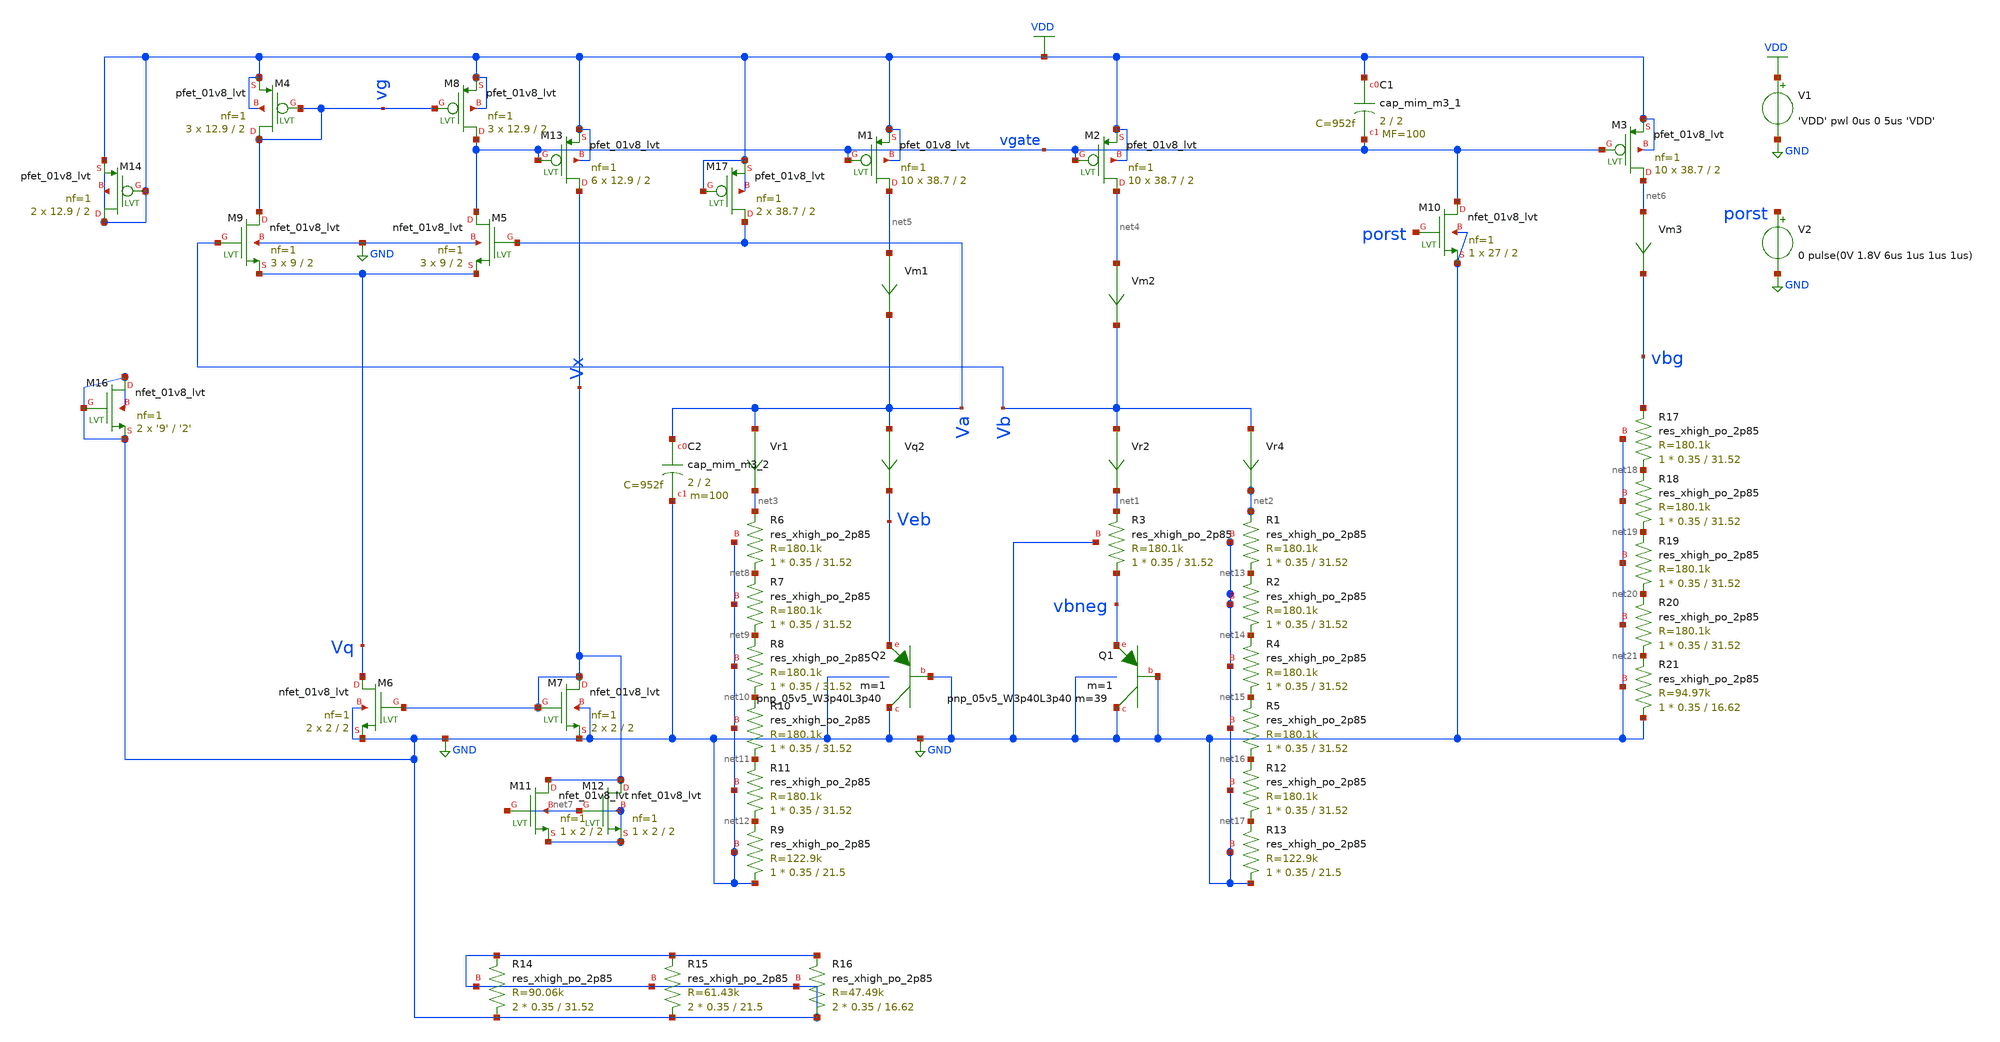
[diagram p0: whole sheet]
** sch_path: schematics/tsmc_bandgap_real_op_layout.sch
**.subckt tsmc_bandgap_real_op_layout
V1 VDD GND 'VDD' pwl 0us 0 5us 'VDD'
XQ2 GND GND Veb sky130_fd_pr__pnp_05v5_W3p40L3p40 m=1
Vr4 Vb net2 0
.save i(vr4)
Vr2 Vb net1 0
.save i(vr2)
Vm1 net5 Va 0
.save i(vm1)
Vm2 net4 Vb 0
.save i(vm2)
Vm3 net6 vbg 0
.save i(vm3)
Vr1 Va net3 0
.save i(vr1)
Vq2 Va Veb 0
.save i(vq2)
XQ1 GND GND vbneg sky130_fd_pr__pnp_05v5_W3p40L3p40 m=39 m=1
XM5 vgate Va Vq GND sky130_fd_pr__nfet_01v8_lvt L=2 W=9 nf=1 ad='int((nf+1)/2) * W/nf * 0.29' as='int((nf+2)/2) * W/nf * 0.29'
+ pd='2*int((nf+1)/2) * (W/nf + 0.29)' ps='2*int((nf+2)/2) * (W/nf + 0.29)' nrd='0.29 / W' nrs='0.29 / W'
+ sa=0 sb=0 sd=0 mult=3 m=3
XM6 Vq Vx GND GND sky130_fd_pr__nfet_01v8_lvt L=2 W=2 nf=1 ad='int((nf+1)/2) * W/nf * 0.29' as='int((nf+2)/2) * W/nf * 0.29'
+ pd='2*int((nf+1)/2) * (W/nf + 0.29)' ps='2*int((nf+2)/2) * (W/nf + 0.29)' nrd='0.29 / W' nrs='0.29 / W'
+ sa=0 sb=0 sd=0 mult=2 m=2
XM9 vg Vb Vq GND sky130_fd_pr__nfet_01v8_lvt L=2 W=9 nf=1 ad='int((nf+1)/2) * W/nf * 0.29' as='int((nf+2)/2) * W/nf * 0.29'
+ pd='2*int((nf+1)/2) * (W/nf + 0.29)' ps='2*int((nf+2)/2) * (W/nf + 0.29)' nrd='0.29 / W' nrs='0.29 / W'
+ sa=0 sb=0 sd=0 mult=3 m=3
XM7 Vx Vx GND GND sky130_fd_pr__nfet_01v8_lvt L=2 W=2 nf=1 ad='int((nf+1)/2) * W/nf * 0.29' as='int((nf+2)/2) * W/nf * 0.29'
+ pd='2*int((nf+1)/2) * (W/nf + 0.29)' ps='2*int((nf+2)/2) * (W/nf + 0.29)' nrd='0.29 / W' nrs='0.29 / W'
+ sa=0 sb=0 sd=0 mult=2 m=2
XM13 Vx vgate VDD VDD sky130_fd_pr__pfet_01v8_lvt L=2 W=12.9 nf=1 ad='int((nf+1)/2) * W/nf * 0.29' as='int((nf+2)/2) * W/nf * 0.29'
+ pd='2*int((nf+1)/2) * (W/nf + 0.29)' ps='2*int((nf+2)/2) * (W/nf + 0.29)' nrd='0.29 / W' nrs='0.29 / W'
+ sa=0 sb=0 sd=0 mult=6 m=6
XM1 net5 vgate VDD VDD sky130_fd_pr__pfet_01v8_lvt L=2 W=38.7 nf=1 ad='int((nf+1)/2) * W/nf * 0.29' as='int((nf+2)/2) * W/nf * 0.29'
+ pd='2*int((nf+1)/2) * (W/nf + 0.29)' ps='2*int((nf+2)/2) * (W/nf + 0.29)' nrd='0.29 / W' nrs='0.29 / W'
+ sa=0 sb=0 sd=0 mult=10 m=10
XM2 net4 vgate VDD VDD sky130_fd_pr__pfet_01v8_lvt L=2 W=38.7 nf=1 ad='int((nf+1)/2) * W/nf * 0.29' as='int((nf+2)/2) * W/nf * 0.29'
+ pd='2*int((nf+1)/2) * (W/nf + 0.29)' ps='2*int((nf+2)/2) * (W/nf + 0.29)' nrd='0.29 / W' nrs='0.29 / W'
+ sa=0 sb=0 sd=0 mult=10 m=10
XM3 net6 vgate VDD VDD sky130_fd_pr__pfet_01v8_lvt L=2 W=38.7 nf=1 ad='int((nf+1)/2) * W/nf * 0.29' as='int((nf+2)/2) * W/nf * 0.29'
+ pd='2*int((nf+1)/2) * (W/nf + 0.29)' ps='2*int((nf+2)/2) * (W/nf + 0.29)' nrd='0.29 / W' nrs='0.29 / W'
+ sa=0 sb=0 sd=0 mult=10 m=10
XM4 vg vg VDD VDD sky130_fd_pr__pfet_01v8_lvt L=2 W=12.9 nf=1 ad='int((nf+1)/2) * W/nf * 0.29' as='int((nf+2)/2) * W/nf * 0.29'
+ pd='2*int((nf+1)/2) * (W/nf + 0.29)' ps='2*int((nf+2)/2) * (W/nf + 0.29)' nrd='0.29 / W' nrs='0.29 / W'
+ sa=0 sb=0 sd=0 mult=3 m=3
XM8 vgate vg VDD VDD sky130_fd_pr__pfet_01v8_lvt L=2 W=12.9 nf=1 ad='int((nf+1)/2) * W/nf * 0.29' as='int((nf+2)/2) * W/nf * 0.29'
+ pd='2*int((nf+1)/2) * (W/nf + 0.29)' ps='2*int((nf+2)/2) * (W/nf + 0.29)' nrd='0.29 / W' nrs='0.29 / W'
+ sa=0 sb=0 sd=0 mult=3 m=3
XM10 vgate porst GND GND sky130_fd_pr__nfet_01v8_lvt L=2 W=27 nf=1 ad='int((nf+1)/2) * W/nf * 0.29' as='int((nf+2)/2) * W/nf * 0.29'
+ pd='2*int((nf+1)/2) * (W/nf + 0.29)' ps='2*int((nf+2)/2) * (W/nf + 0.29)' nrd='0.29 / W' nrs='0.29 / W'
+ sa=0 sb=0 sd=0 mult=1 m=1
V2 porst GND 0 pulse(0V 1.8V 6us 1us 1us 1us)
XR6 net8 net3 GND sky130_fd_pr__res_xhigh_po_2p85 L=31.52 mult=1 m=1
XR7 net9 net8 GND sky130_fd_pr__res_xhigh_po_2p85 L=31.52 mult=1 m=1
XR8 net10 net9 GND sky130_fd_pr__res_xhigh_po_2p85 L=31.52 mult=1 m=1
XR10 net11 net10 GND sky130_fd_pr__res_xhigh_po_2p85 L=31.52 mult=1 m=1
XR11 net12 net11 GND sky130_fd_pr__res_xhigh_po_2p85 L=31.52 mult=1 m=1
XR9 GND net12 GND sky130_fd_pr__res_xhigh_po_2p85 L=21.5 mult=1 m=1
XR3 vbneg net1 GND sky130_fd_pr__res_xhigh_po_2p85 L=31.52 mult=1 m=1
XR1 net13 net2 GND sky130_fd_pr__res_xhigh_po_2p85 L=31.52 mult=1 m=1
XR2 net14 net13 GND sky130_fd_pr__res_xhigh_po_2p85 L=31.52 mult=1 m=1
XR4 net15 net14 GND sky130_fd_pr__res_xhigh_po_2p85 L=31.52 mult=1 m=1
XR5 net16 net15 GND sky130_fd_pr__res_xhigh_po_2p85 L=31.52 mult=1 m=1
XR12 net17 net16 GND sky130_fd_pr__res_xhigh_po_2p85 L=31.52 mult=1 m=1
XR13 GND net17 GND sky130_fd_pr__res_xhigh_po_2p85 L=21.5 mult=1 m=1
XR17 net18 vbg GND sky130_fd_pr__res_xhigh_po_2p85 L=31.52 mult=1 m=1
XR18 net19 net18 GND sky130_fd_pr__res_xhigh_po_2p85 L=31.52 mult=1 m=1
XR19 net20 net19 GND sky130_fd_pr__res_xhigh_po_2p85 L=31.52 mult=1 m=1
XR20 net21 net20 GND sky130_fd_pr__res_xhigh_po_2p85 L=31.52 mult=1 m=1
XR21 GND net21 GND sky130_fd_pr__res_xhigh_po_2p85 L=16.62 mult=1 m=1
XC1 VDD vgate sky130_fd_pr__cap_mim_m3_1 W=2 L=2 MF=100 m=100
XC2 Va GND sky130_fd_pr__cap_mim_m3_2 W=2 L=2 MF=100 m=100
XR14 GND GND GND sky130_fd_pr__res_xhigh_po_2p85 L=31.52 mult=2 m=2
XR15 GND GND GND sky130_fd_pr__res_xhigh_po_2p85 L=21.5 mult=2 m=2
XR16 GND GND GND sky130_fd_pr__res_xhigh_po_2p85 L=16.62 mult=2 m=2
XM11 Vx net7 net7 net7 sky130_fd_pr__nfet_01v8_lvt L=2 W=2 nf=1 ad='int((nf+1)/2) * W/nf * 0.29' as='int((nf+2)/2) * W/nf * 0.29'
+ pd='2*int((nf+1)/2) * (W/nf + 0.29)' ps='2*int((nf+2)/2) * (W/nf + 0.29)' nrd='0.29 / W' nrs='0.29 / W'
+ sa=0 sb=0 sd=0 mult=1 m=1
XM12 Vx net7 net7 net7 sky130_fd_pr__nfet_01v8_lvt L=2 W=2 nf=1 ad='int((nf+1)/2) * W/nf * 0.29' as='int((nf+2)/2) * W/nf * 0.29'
+ pd='2*int((nf+1)/2) * (W/nf + 0.29)' ps='2*int((nf+2)/2) * (W/nf + 0.29)' nrd='0.29 / W' nrs='0.29 / W'
+ sa=0 sb=0 sd=0 mult=1 m=1
XM14 VDD VDD VDD VDD sky130_fd_pr__pfet_01v8_lvt L=2 W=12.9 nf=1 ad='int((nf+1)/2) * W/nf * 0.29' as='int((nf+2)/2) * W/nf * 0.29'
+ pd='2*int((nf+1)/2) * (W/nf + 0.29)' ps='2*int((nf+2)/2) * (W/nf + 0.29)' nrd='0.29 / W' nrs='0.29 / W'
+ sa=0 sb=0 sd=0 mult=2 m=2
XM16 GND GND GND GND sky130_fd_pr__nfet_01v8_lvt L='2' W='9' nf=1 ad='int((nf+1)/2) * W/nf * 0.29' as='int((nf+2)/2) * W/nf * 0.29'
+ pd='2*int((nf+1)/2) * (W/nf + 0.29)' ps='2*int((nf+2)/2) * (W/nf + 0.29)' nrd='0.29 / W' nrs='0.29 / W'
+ sa=0 sb=0 sd=0 mult=2 m=2
XM17 Va VDD VDD VDD sky130_fd_pr__pfet_01v8_lvt L=2 W=38.7 nf=1 ad='int((nf+1)/2) * W/nf * 0.29' as='int((nf+2)/2) * W/nf * 0.29'
+ pd='2*int((nf+1)/2) * (W/nf + 0.29)' ps='2*int((nf+2)/2) * (W/nf + 0.29)' nrd='0.29 / W' nrs='0.29 / W'
+ sa=0 sb=0 sd=0 mult=2 m=2
**** begin user architecture code

.include $::SKYWATER_MODELS/cells/nfet_01v8/sky130_fd_pr__nfet_01v8__tt.corner.spice
.include $::SKYWATER_MODELS/cells/nfet_01v8_lvt/sky130_fd_pr__nfet_01v8_lvt__tt.corner.spice
.include $::SKYWATER_MODELS/cells/pfet_01v8/sky130_fd_pr__pfet_01v8__tt.corner.spice
.include $::SKYWATER_MODELS/cells/nfet_03v3_nvt/sky130_fd_pr__nfet_03v3_nvt__tt.corner.spice
.include $::SKYWATER_MODELS/cells/nfet_05v0_nvt/sky130_fd_pr__nfet_05v0_nvt__tt.corner.spice
.include $::SKYWATER_MODELS/cells/esd_nfet_01v8/sky130_fd_pr__esd_nfet_01v8__tt.corner.spice
.include $::SKYWATER_MODELS/cells/pfet_01v8_lvt/sky130_fd_pr__pfet_01v8_lvt__tt.corner.spice
.include $::SKYWATER_MODELS/cells/pfet_01v8_hvt/sky130_fd_pr__pfet_01v8_hvt__tt.corner.spice
.include $::SKYWATER_MODELS/cells/esd_pfet_g5v0d10v5/sky130_fd_pr__esd_pfet_g5v0d10v5__tt.corner.spice
.include $::SKYWATER_MODELS/cells/pfet_g5v0d10v5/sky130_fd_pr__pfet_g5v0d10v5__tt.corner.spice
.include $::SKYWATER_MODELS/cells/pfet_g5v0d16v0/sky130_fd_pr__pfet_g5v0d16v0__tt.corner.spice
.include $::SKYWATER_MODELS/cells/nfet_g5v0d10v5/sky130_fd_pr__nfet_g5v0d10v5__tt.corner.spice
.include $::SKYWATER_MODELS/cells/nfet_g5v0d16v0/sky130_fd_pr__nfet_g5v0d16v0__tt_discrete.corner.spice
.include $::SKYWATER_MODELS/cells/esd_nfet_g5v0d10v5/sky130_fd_pr__esd_nfet_g5v0d10v5__tt.corner.spice
.include $::SKYWATER_MODELS/models/corners/tt/nonfet.spice
* Mismatch parameters
.include $::SKYWATER_MODELS/cells/nfet_01v8/sky130_fd_pr__nfet_01v8__mismatch.corner.spice
.include $::SKYWATER_MODELS/cells/pfet_01v8/sky130_fd_pr__pfet_01v8__mismatch.corner.spice
.include $::SKYWATER_MODELS/cells/nfet_01v8_lvt/sky130_fd_pr__nfet_01v8_lvt__mismatch.corner.spice
.include $::SKYWATER_MODELS/cells/pfet_01v8_lvt/sky130_fd_pr__pfet_01v8_lvt__mismatch.corner.spice
.include $::SKYWATER_MODELS/cells/pfet_01v8_hvt/sky130_fd_pr__pfet_01v8_hvt__mismatch.corner.spice
.include $::SKYWATER_MODELS/cells/nfet_g5v0d10v5/sky130_fd_pr__nfet_g5v0d10v5__mismatch.corner.spice
.include $::SKYWATER_MODELS/cells/pfet_g5v0d10v5/sky130_fd_pr__pfet_g5v0d10v5__mismatch.corner.spice
.include $::SKYWATER_MODELS/cells/nfet_05v0_nvt/sky130_fd_pr__nfet_05v0_nvt__mismatch.corner.spice
.include $::SKYWATER_MODELS/cells/nfet_03v3_nvt/sky130_fd_pr__nfet_03v3_nvt__mismatch.corner.spice
* Resistor$::SKYWATER_MODELS/Capacitor
.include $::SKYWATER_MODELS/models/r+c/res_typical__cap_typical.spice
.include $::SKYWATER_MODELS/models/r+c/res_typical__cap_typical__lin.spice
* Special cells
.include $::SKYWATER_MODELS/models/corners/tt/specialized_cells.spice
* All models
.include $::SKYWATER_MODELS/models/all.spice
*.include $::SKYWATER_MODELS/cells/pnp_05v5/sky130_fd_pr__pnp_05v5_W3p40L3p40.model.spice
.include /tmp/kustinj/ee272bclone/open_pdks/sky130A/libs.ref/sky130_fd_pr/spice/sky130_fd_pr__pnp_05v5_W3p40L3p40.model.spice
* Corner
.include $::SKYWATER_MODELS/models/corners/tt/rf.spice



.ic V(vgate)=0
.ic V(vg)=0
.option savecurrents
.param mc_mm_switch=0
.param R3val='22.187k'
.param alpha='1'
.param R2R3ratio='5.6555038*alpha'
.param R2val='R3val*R2R3ratio'
.param R4R2ratio='0.79694273'
.param R4val='R2val*R4R2ratio
.param VDD=1.8
.control
save all  @m.xm1.msky130_fd_pr__pfet_01v8_lvt[gm]  @m.xm2.msky130_fd_pr__pfet_01v8_lvt[gm]  @m.xm3.msky130_fd_pr__pfet_01v8_lvt[gm]  @m.xm4.msky130_fd_pr__pfet_01v8_lvt[gm]  @m.xm5.msky130_fd_pr__nfet_01v8_lvt[gm]  @m.xm6.msky130_fd_pr__nfet_01v8_lvt[gm]  @m.xm7.msky130_fd_pr__nfet_01v8_lvt[gm]  @m.xm8.msky130_fd_pr__pfet_01v8_lvt[gm]  @m.xm9.msky130_fd_pr__nfet_01v8_lvt[gm]  @m.xm13.msky130_fd_pr__pfet_01v8_lvt[gm]

option temp=27
tran 1n 11u
option temp=0
tran 1n 11u
option temp=70
tran 1n 11u
*write ./sims/tsmc_bandgap_real_layout_70degc_vbg.raw vbg
*setplot tran2
*write ./sims/tsmc_bandgap_real_layout_0degc_vbg.raw vbg
*setplot tran1
*write ./sims/tsmc_bandgap_real_layout_27degc_vbg.raw vbg
*unset askquit
*quit
.endc


**** end user architecture code
**.ends
.GLOBAL VDD
.GLOBAL GND
.end
